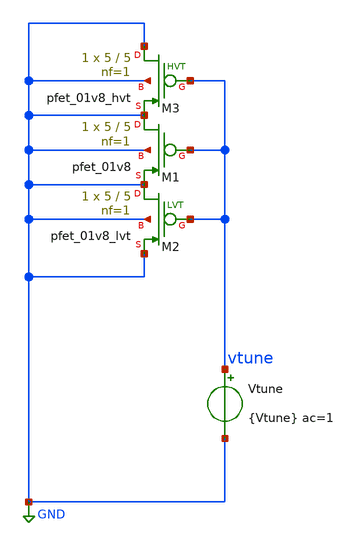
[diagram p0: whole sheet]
** sch_path: research/varactor/varactor_ac.sch
**.subckt varactor_ac
Vtune vtune GND {Vtune} ac=1
XM1 GND vtune GND GND sky130_fd_pr__pfet_01v8 L=5 W=5 nf=1 ad='int((nf+1)/2) * W/nf * 0.29' as='int((nf+2)/2) * W/nf * 0.29'
+ pd='2*int((nf+1)/2) * (W/nf + 0.29)' ps='2*int((nf+2)/2) * (W/nf + 0.29)' nrd='0.29 / W' nrs='0.29 / W'
+ sa=0 sb=0 sd=0 mult=1 m=1
XM2 GND vtune GND GND sky130_fd_pr__pfet_01v8_lvt L=5 W=5 nf=1 ad='int((1 + 1)/2) * 5 / 1 * 0.29' as='int((1 + 2)/2) * 5 / 1 * 0.29'
+ pd='2*int((1 + 1)/2) * (5 / 1 + 0.29)' ps='2*int((1 + 2)/2) * (5 / 1 + 0.29)' nrd='0.29 / 5 ' nrs='0.29 / 5 '
+ sa=0 sb=0 sd=0 mult=1 m=1
XM3 GND vtune GND GND sky130_fd_pr__pfet_01v8_hvt L=5 W=5 nf=1 ad='int((1 + 1)/2) * 5 / 1 * 0.29' as='int((1 + 2)/2) * 5 / 1 * 0.29'
+ pd='2*int((1 + 1)/2) * (5 / 1 + 0.29)' ps='2*int((1 + 2)/2) * (5 / 1 + 0.29)' nrd='0.29 / 5 ' nrs='0.29 / 5 '
+ sa=0 sb=0 sd=0 mult=1 m=1
**** begin user architecture code


.param temp=27
.param vtune=0.2
.lib sky130_fd_pr/models/sky130.lib.spice tt
.inc sky130_fd_pr/cells/cap_var_hvt/sky130_fd_pr__cap_var_hvt.model.spice
.ac dec 10 10 100e9

.control

plot vtune#branch

*let Vtune=0.0
*while length le 8u ; problem occurs when changed to 9u
*    alter @m[l] length
*    print length cnt
*    save @m[id] @m[gds]
*    dc vds 0 1.8 0.05 vgs 0 1.8 0.05
*    wrdata output/$&cnt @m[id]/@m[gds]
*    let length=length+0.1u
*end
.endc


**** end user architecture code
**.ends
.GLOBAL GND
.end
